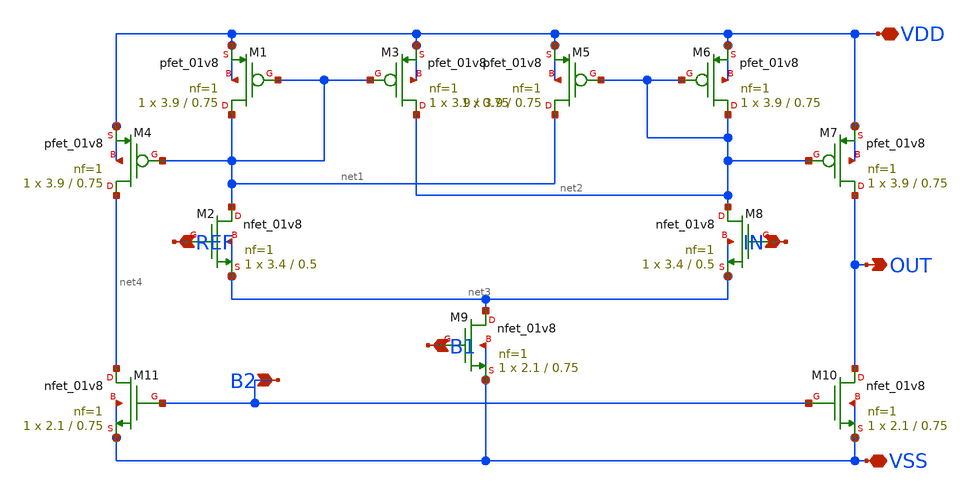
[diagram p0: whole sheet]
** sch_path: cmos_comparator/komparator_histeris.sch
**.subckt komparator_histeris VDD VSS IN REF B2 B1 OUT
*.iopin VDD
*.iopin VSS
*.ipin IN
*.ipin REF
*.ipin B2
*.ipin B1
*.opin OUT
XM1 net1 net1 VDD VDD sky130_fd_pr__pfet_01v8 L=0.75 W=3.9 nf=1 ad='int((1 + 1)/2) * 3.9 / 1 * 0.29'
+ as='int((1 + 2)/2) * 3.9 / 1 * 0.29' pd='2*int((1 + 1)/2) * (3.9 / 1 + 0.29)' ps='2*int((1 + 2)/2) * (3.9 / 1 + 0.29)'
+ nrd='0.29 / 3.9 ' nrs='0.29 / 3.9 ' sa=0 sb=0 sd=0 mult=1 m=1
XM2 net1 REF net3 net3 sky130_fd_pr__nfet_01v8 L=0.5 W=3.4 nf=1 ad='int((1 + 1)/2) * 3.4 / 1 * 0.29'
+ as='int((1 + 2)/2) * 3.4 / 1 * 0.29' pd='2*int((1 + 1)/2) * (3.4 / 1 + 0.29)' ps='2*int((1 + 2)/2) * (3.4 / 1 + 0.29)'
+ nrd='0.29 / 3.4 ' nrs='0.29 / 3.4 ' sa=0 sb=0 sd=0 mult=1 m=1
XM3 net2 net1 VDD VDD sky130_fd_pr__pfet_01v8 L=0.75 W=3.9 nf=1 ad='int((1 + 1)/2) * 3.9 / 1 * 0.29'
+ as='int((1 + 2)/2) * 3.9 / 1 * 0.29' pd='2*int((1 + 1)/2) * (3.9 / 1 + 0.29)' ps='2*int((1 + 2)/2) * (3.9 / 1 + 0.29)'
+ nrd='0.29 / 3.9 ' nrs='0.29 / 3.9 ' sa=0 sb=0 sd=0 mult=1 m=1
XM4 net4 net1 VDD VDD sky130_fd_pr__pfet_01v8 L=0.75 W=3.9 nf=1 ad='int((1 + 1)/2) * 3.9 / 1 * 0.29'
+ as='int((1 + 2)/2) * 3.9 / 1 * 0.29' pd='2*int((1 + 1)/2) * (3.9 / 1 + 0.29)' ps='2*int((1 + 2)/2) * (3.9 / 1 + 0.29)'
+ nrd='0.29 / 3.9 ' nrs='0.29 / 3.9 ' sa=0 sb=0 sd=0 mult=1 m=1
XM5 net1 net2 VDD VDD sky130_fd_pr__pfet_01v8 L=0.75 W=3.9 nf=1 ad='int((1 + 1)/2) * 3.9 / 1 * 0.29'
+ as='int((1 + 2)/2) * 3.9 / 1 * 0.29' pd='2*int((1 + 1)/2) * (3.9 / 1 + 0.29)' ps='2*int((1 + 2)/2) * (3.9 / 1 + 0.29)'
+ nrd='0.29 / 3.9 ' nrs='0.29 / 3.9 ' sa=0 sb=0 sd=0 mult=1 m=1
XM6 net2 net2 VDD VDD sky130_fd_pr__pfet_01v8 L=0.75 W=3.9 nf=1 ad='int((1 + 1)/2) * 3.9 / 1 * 0.29'
+ as='int((1 + 2)/2) * 3.9 / 1 * 0.29' pd='2*int((1 + 1)/2) * (3.9 / 1 + 0.29)' ps='2*int((1 + 2)/2) * (3.9 / 1 + 0.29)'
+ nrd='0.29 / 3.9 ' nrs='0.29 / 3.9 ' sa=0 sb=0 sd=0 mult=1 m=1
XM7 OUT net2 VDD VDD sky130_fd_pr__pfet_01v8 L=0.75 W=3.9 nf=1 ad='int((1 + 1)/2) * 3.9 / 1 * 0.29' as='int((1 + 2)/2) * 3.9 / 1 * 0.29'
+ pd='2*int((1 + 1)/2) * (3.9 / 1 + 0.29)' ps='2*int((1 + 2)/2) * (3.9 / 1 + 0.29)' nrd='0.29 / 3.9 ' nrs='0.29 / 3.9 '
+ sa=0 sb=0 sd=0 mult=1 m=1
XM8 net2 IN net3 net3 sky130_fd_pr__nfet_01v8 L=0.5 W=3.4 nf=1 ad='int((1 + 1)/2) * 3.4 / 1 * 0.29' as='int((1 + 2)/2) * 3.4 / 1 * 0.29'
+ pd='2*int((1 + 1)/2) * (3.4 / 1 + 0.29)' ps='2*int((1 + 2)/2) * (3.4 / 1 + 0.29)' nrd='0.29 / 3.4 ' nrs='0.29 / 3.4 '
+ sa=0 sb=0 sd=0 mult=1 m=1
XM9 net3 B1 VSS VSS sky130_fd_pr__nfet_01v8 L=0.75 W=2.1 nf=1 ad='int((1 + 1)/2) * 2.1 / 1 * 0.29' as='int((1 + 2)/2) * 2.1 / 1 * 0.29'
+ pd='2*int((1 + 1)/2) * (2.1 / 1 + 0.29)' ps='2*int((1 + 2)/2) * (2.1 / 1 + 0.29)' nrd='0.29 / 2.1 ' nrs='0.29 / 2.1 '
+ sa=0 sb=0 sd=0 mult=1 m=1
XM10 OUT B2 VSS VSS sky130_fd_pr__nfet_01v8 L=0.75 W=2.1 nf=1 ad='int((1 + 1)/2) * 2.1 / 1 * 0.29' as='int((1 + 2)/2) * 2.1 / 1 * 0.29'
+ pd='2*int((1 + 1)/2) * (2.1 / 1 + 0.29)' ps='2*int((1 + 2)/2) * (2.1 / 1 + 0.29)' nrd='0.29 / 2.1 ' nrs='0.29 / 2.1 '
+ sa=0 sb=0 sd=0 mult=1 m=1
XM11 net4 B2 VSS VSS sky130_fd_pr__nfet_01v8 L=0.75 W=2.1 nf=1 ad='int((1 + 1)/2) * 2.1 / 1 * 0.29' as='int((1 + 2)/2) * 2.1 / 1 * 0.29'
+ pd='2*int((1 + 1)/2) * (2.1 / 1 + 0.29)' ps='2*int((1 + 2)/2) * (2.1 / 1 + 0.29)' nrd='0.29 / 2.1 ' nrs='0.29 / 2.1 '
+ sa=0 sb=0 sd=0 mult=1 m=1
**.ends
.end
